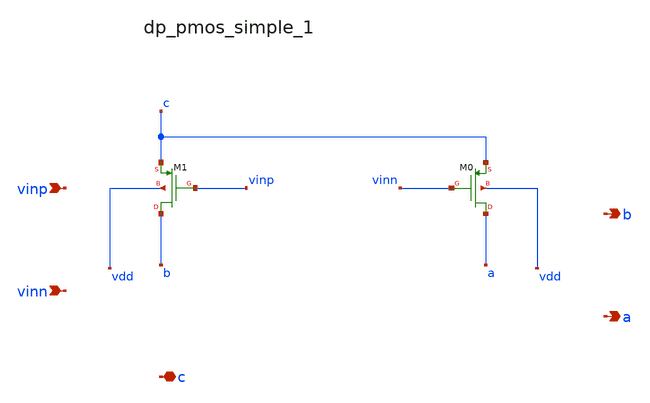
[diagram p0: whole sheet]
** sch_path: analog-db/raw/amp_022_fer_two_stage/hier/blocks/dp_pmos_simple_1.sch
**.subckt dp_pmos_simple_1 vinp vinn c b a
*.ipin vinp
*.ipin vinn
*.iopin c
*.opin b
*.opin a
XM0 a vinn c vdd sg13_lv_pmos w=x_dut_xm0_w l=x_dut_xm0_l ng=1 m=x_dut_xm0_m
XM1 b vinp c vdd sg13_lv_pmos w=x_dut_xm1_w l=x_dut_xm1_l ng=1 m=x_dut_xm1_m
**.ends
.end
